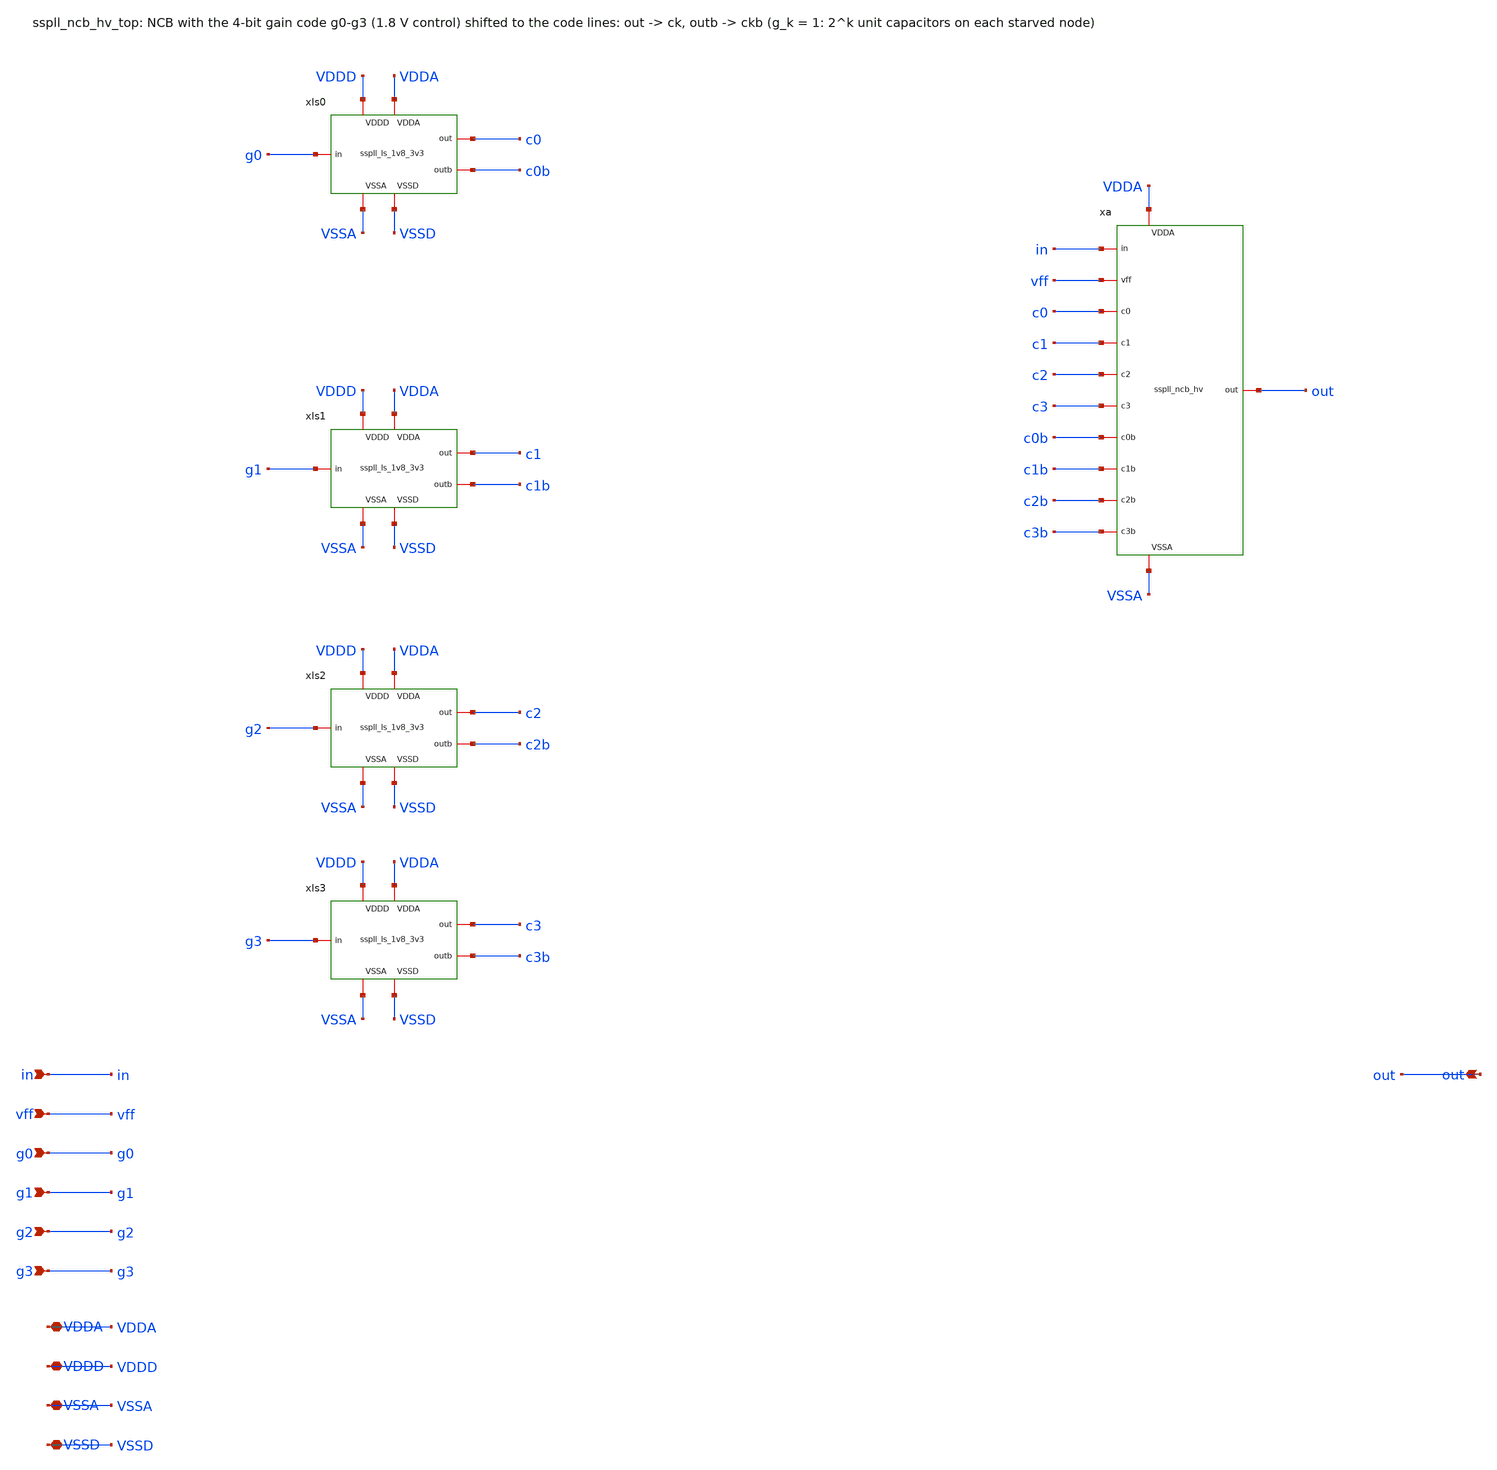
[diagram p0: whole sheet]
** sch_path: xschem/ncb_hv/sspll_ncb_hv_top.sch
**.subckt sspll_ncb_hv_top in vff g0 g1 g2 g3 out VDDA VDDD VSSA VSSD
*.ipin in
*.ipin vff
*.ipin g0
*.ipin g1
*.ipin g2
*.ipin g3
*.opin out
*.iopin VDDA
*.iopin VDDD
*.iopin VSSA
*.iopin VSSD
xls0 g0 c0 c0b VDDD VDDA VSSA VSSD sspll_ls_1v8_3v3
xls1 g1 c1 c1b VDDD VDDA VSSA VSSD sspll_ls_1v8_3v3
xls2 g2 c2 c2b VDDD VDDA VSSA VSSD sspll_ls_1v8_3v3
xls3 g3 c3 c3b VDDD VDDA VSSA VSSD sspll_ls_1v8_3v3
xa in vff c0 c1 c2 c3 c0b c1b c2b c3b out VDDA VSSA sspll_ncb_hv
**.ends

* expanding   symbol:  ../cco_hv/sspll_ls_1v8_3v3.sym # of pins=7
** sym_path: xschem/cco_hv/sspll_ls_1v8_3v3.sym
** sch_path: xschem/cco_hv/sspll_ls_1v8_3v3.sch
.subckt sspll_ls_1v8_3v3 in out outb VDDD VDDA VSSA VSSD
*.iopin VDDD
*.iopin VDDA
*.iopin VSSD
*.iopin VSSA
*.ipin in
*.opin outb
*.opin out
XXPI net1 in VDDD VDDD sky130_fd_pr__pfet_01v8 L=0.15 W=1 nf=1 ad='int((nf+1)/2) * W/nf * 0.29' as='int((nf+2)/2) * W/nf * 0.29'
+ pd='2*int((nf+1)/2) * (W/nf + 0.29)' ps='2*int((nf+2)/2) * (W/nf + 0.29)' nrd='0.29 / W' nrs='0.29 / W'
+ sa=0 sb=0 sd=0 mult=1 m=1
XXNI net1 in VSSD VSSD sky130_fd_pr__nfet_01v8 L=0.15 W=0.5 nf=1 ad='int((nf+1)/2) * W/nf * 0.29' as='int((nf+2)/2) * W/nf * 0.29'
+ pd='2*int((nf+1)/2) * (W/nf + 0.29)' ps='2*int((nf+2)/2) * (W/nf + 0.29)' nrd='0.29 / W' nrs='0.29 / W'
+ sa=0 sb=0 sd=0 mult=1 m=1
XXP1 net2 net3 VDDA VDDA sky130_fd_pr__pfet_g5v0d10v5 L=0.5 W=1 nf=1 ad='int((nf+1)/2) * W/nf * 0.29'
+ as='int((nf+2)/2) * W/nf * 0.29' pd='2*int((nf+1)/2) * (W/nf + 0.29)' ps='2*int((nf+2)/2) * (W/nf + 0.29)'
+ nrd='0.29 / W' nrs='0.29 / W' sa=0 sb=0 sd=0 mult=1 m=1
XXP2 net3 net2 VDDA VDDA sky130_fd_pr__pfet_g5v0d10v5 L=0.5 W=1 nf=1 ad='int((nf+1)/2) * W/nf * 0.29'
+ as='int((nf+2)/2) * W/nf * 0.29' pd='2*int((nf+1)/2) * (W/nf + 0.29)' ps='2*int((nf+2)/2) * (W/nf + 0.29)'
+ nrd='0.29 / W' nrs='0.29 / W' sa=0 sb=0 sd=0 mult=1 m=1
XXN1 net2 in VSSA VSSA sky130_fd_pr__nfet_g5v0d10v5 L=0.5 W=3 nf=1 ad='int((nf+1)/2) * W/nf * 0.29' as='int((nf+2)/2) * W/nf * 0.29'
+ pd='2*int((nf+1)/2) * (W/nf + 0.29)' ps='2*int((nf+2)/2) * (W/nf + 0.29)' nrd='0.29 / W' nrs='0.29 / W'
+ sa=0 sb=0 sd=0 mult=1 m=1
XXN2 net3 net1 VSSA VSSA sky130_fd_pr__nfet_g5v0d10v5 L=0.5 W=3 nf=1 ad='int((nf+1)/2) * W/nf * 0.29'
+ as='int((nf+2)/2) * W/nf * 0.29' pd='2*int((nf+1)/2) * (W/nf + 0.29)' ps='2*int((nf+2)/2) * (W/nf + 0.29)'
+ nrd='0.29 / W' nrs='0.29 / W' sa=0 sb=0 sd=0 mult=1 m=1
XXPB outb net3 VDDA VDDA sky130_fd_pr__pfet_g5v0d10v5 L=0.5 W=2 nf=1 ad='int((nf+1)/2) * W/nf * 0.29'
+ as='int((nf+2)/2) * W/nf * 0.29' pd='2*int((nf+1)/2) * (W/nf + 0.29)' ps='2*int((nf+2)/2) * (W/nf + 0.29)'
+ nrd='0.29 / W' nrs='0.29 / W' sa=0 sb=0 sd=0 mult=1 m=1
XXNB outb net3 VSSA VSSA sky130_fd_pr__nfet_g5v0d10v5 L=0.5 W=1 nf=1 ad='int((nf+1)/2) * W/nf * 0.29'
+ as='int((nf+2)/2) * W/nf * 0.29' pd='2*int((nf+1)/2) * (W/nf + 0.29)' ps='2*int((nf+2)/2) * (W/nf + 0.29)'
+ nrd='0.29 / W' nrs='0.29 / W' sa=0 sb=0 sd=0 mult=1 m=1
XXPO out net2 VDDA VDDA sky130_fd_pr__pfet_g5v0d10v5 L=0.5 W=2 nf=1 ad='int((nf+1)/2) * W/nf * 0.29'
+ as='int((nf+2)/2) * W/nf * 0.29' pd='2*int((nf+1)/2) * (W/nf + 0.29)' ps='2*int((nf+2)/2) * (W/nf + 0.29)'
+ nrd='0.29 / W' nrs='0.29 / W' sa=0 sb=0 sd=0 mult=1 m=1
XXNO out net2 VSSA VSSA sky130_fd_pr__nfet_g5v0d10v5 L=0.5 W=1 nf=1 ad='int((nf+1)/2) * W/nf * 0.29'
+ as='int((nf+2)/2) * W/nf * 0.29' pd='2*int((nf+1)/2) * (W/nf + 0.29)' ps='2*int((nf+2)/2) * (W/nf + 0.29)'
+ nrd='0.29 / W' nrs='0.29 / W' sa=0 sb=0 sd=0 mult=1 m=1
.ends


* expanding   symbol:  sspll_ncb_hv.sym # of pins=13
** sym_path: xschem/ncb_hv/sspll_ncb_hv.sym
** sch_path: xschem/ncb_hv/sspll_ncb_hv.sch
.subckt sspll_ncb_hv in vff c0 c1 c2 c3 c0b c1b c2b c3b out VDDA VSSA
*.ipin in
*.ipin vff
*.ipin c0
*.ipin c1
*.ipin c2
*.ipin c3
*.ipin c0b
*.ipin c1b
*.ipin c2b
*.ipin c3b
*.opin out
*.iopin VDDA
*.iopin VSSA
xb vff nb pd VDDA VSSA sspll_ncb_hv_bias
xl in nb pd c0 c1 c2 c3 c0b c1b c2b c3b out VDDA VSSA sspll_ncb_hv_line
.ends


* expanding   symbol:  sspll_ncb_hv_bias.sym # of pins=5
** sym_path: xschem/ncb_hv/sspll_ncb_hv_bias.sym
** sch_path: xschem/ncb_hv/sspll_ncb_hv_bias.sch
.subckt sspll_ncb_hv_bias vff nb pd VDDA VSSA
*.ipin vff
*.opin nb
*.opin pd
*.iopin VDDA
*.iopin VSSA
XXPD pd pd VDDA VDDA sky130_fd_pr__pfet_g5v0d10v5 L=0.5 W=4 nf=1 ad='int((nf+1)/2) * W/nf * 0.29' as='int((nf+2)/2) * W/nf * 0.29'
+ pd='2*int((nf+1)/2) * (W/nf + 0.29)' ps='2*int((nf+2)/2) * (W/nf + 0.29)' nrd='0.29 / W' nrs='0.29 / W'
+ sa=0 sb=0 sd=0 mult=1 m=1
XXI pd vff VSSA VSSA sky130_fd_pr__nfet_g5v0d10v5 L=1.0 W=2 nf=1 ad='int((nf+1)/2) * W/nf * 0.29' as='int((nf+2)/2) * W/nf * 0.29'
+ pd='2*int((nf+1)/2) * (W/nf + 0.29)' ps='2*int((nf+2)/2) * (W/nf + 0.29)' nrd='0.29 / W' nrs='0.29 / W'
+ sa=0 sb=0 sd=0 mult=1 m=1
XXPO nb pd VDDA VDDA sky130_fd_pr__pfet_g5v0d10v5 L=0.5 W=4 nf=1 ad='int((nf+1)/2) * W/nf * 0.29' as='int((nf+2)/2) * W/nf * 0.29'
+ pd='2*int((nf+1)/2) * (W/nf + 0.29)' ps='2*int((nf+2)/2) * (W/nf + 0.29)' nrd='0.29 / W' nrs='0.29 / W'
+ sa=0 sb=0 sd=0 mult=1 m=1
XXND nb nb VSSA VSSA sky130_fd_pr__nfet_g5v0d10v5 L=0.5 W=2 nf=1 ad='int((nf+1)/2) * W/nf * 0.29' as='int((nf+2)/2) * W/nf * 0.29'
+ pd='2*int((nf+1)/2) * (W/nf + 0.29)' ps='2*int((nf+2)/2) * (W/nf + 0.29)' nrd='0.29 / W' nrs='0.29 / W'
+ sa=0 sb=0 sd=0 mult=1 m=1
.ends


* expanding   symbol:  sspll_ncb_hv_line.sym # of pins=14
** sym_path: xschem/ncb_hv/sspll_ncb_hv_line.sym
** sch_path: xschem/ncb_hv/sspll_ncb_hv_line.sch
.subckt sspll_ncb_hv_line in nb pd c0 c1 c2 c3 c0b c1b c2b c3b out VDDA VSSA
*.opin out
*.ipin in
*.ipin nb
*.ipin pd
*.ipin c0
*.ipin c1
*.ipin c2
*.ipin c3
*.ipin c0b
*.ipin c1b
*.ipin c2b
*.ipin c3b
*.iopin VDDA
*.iopin VSSA
x1 net1 nb pd a VDDA VSSA sspll_ncb_hv_sinv
x2 a nb pd b VDDA VSSA sspll_ncb_hv_sinv
XX0P net1 in VDDA VDDA sky130_fd_pr__pfet_g5v0d10v5 L=0.5 W=2.5 nf=1 ad='int((nf+1)/2) * W/nf * 0.29'
+ as='int((nf+2)/2) * W/nf * 0.29' pd='2*int((nf+1)/2) * (W/nf + 0.29)' ps='2*int((nf+2)/2) * (W/nf + 0.29)'
+ nrd='0.29 / W' nrs='0.29 / W' sa=0 sb=0 sd=0 mult=1 m=1
XX0N net1 in VSSA VSSA sky130_fd_pr__nfet_g5v0d10v5 L=0.5 W=1 nf=1 ad='int((nf+1)/2) * W/nf * 0.29' as='int((nf+2)/2) * W/nf * 0.29'
+ pd='2*int((nf+1)/2) * (W/nf + 0.29)' ps='2*int((nf+2)/2) * (W/nf + 0.29)' nrd='0.29 / W' nrs='0.29 / W'
+ sa=0 sb=0 sd=0 mult=1 m=1
xba a c0 c1 c2 c3 c0b c1b c2b c3b VDDA VSSA sspll_ncb_hv_bank
xbb b c0 c1 c2 c3 c0b c1b c2b c3b VDDA VSSA sspll_ncb_hv_bank
XX3P out b VDDA VDDA sky130_fd_pr__pfet_g5v0d10v5 L=0.5 W=5 nf=1 ad='int((nf+1)/2) * W/nf * 0.29' as='int((nf+2)/2) * W/nf * 0.29'
+ pd='2*int((nf+1)/2) * (W/nf + 0.29)' ps='2*int((nf+2)/2) * (W/nf + 0.29)' nrd='0.29 / W' nrs='0.29 / W'
+ sa=0 sb=0 sd=0 mult=1 m=1
XX3N out b VSSA VSSA sky130_fd_pr__nfet_g5v0d10v5 L=0.5 W=2 nf=1 ad='int((nf+1)/2) * W/nf * 0.29' as='int((nf+2)/2) * W/nf * 0.29'
+ pd='2*int((nf+1)/2) * (W/nf + 0.29)' ps='2*int((nf+2)/2) * (W/nf + 0.29)' nrd='0.29 / W' nrs='0.29 / W'
+ sa=0 sb=0 sd=0 mult=1 m=1
.ends


* expanding   symbol:  sspll_ncb_hv_sinv.sym # of pins=6
** sym_path: xschem/ncb_hv/sspll_ncb_hv_sinv.sym
** sch_path: xschem/ncb_hv/sspll_ncb_hv_sinv.sch
.subckt sspll_ncb_hv_sinv i nb pd o VDDA VSSA
*.opin o
*.ipin i
*.ipin nb
*.ipin pd
*.iopin VDDA
*.iopin VSSA
XXSP net1 pd VDDA VDDA sky130_fd_pr__pfet_g5v0d10v5 L=0.5 W=4 nf=1 ad='int((nf+1)/2) * W/nf * 0.29' as='int((nf+2)/2) * W/nf * 0.29'
+ pd='2*int((nf+1)/2) * (W/nf + 0.29)' ps='2*int((nf+2)/2) * (W/nf + 0.29)' nrd='0.29 / W' nrs='0.29 / W'
+ sa=0 sb=0 sd=0 mult=30 m=30
XXP o i net1 VDDA sky130_fd_pr__pfet_g5v0d10v5 L=0.5 W=8 nf=1 ad='int((nf+1)/2) * W/nf * 0.29' as='int((nf+2)/2) * W/nf * 0.29'
+ pd='2*int((nf+1)/2) * (W/nf + 0.29)' ps='2*int((nf+2)/2) * (W/nf + 0.29)' nrd='0.29 / W' nrs='0.29 / W'
+ sa=0 sb=0 sd=0 mult=1 m=1
XXN o i net2 VSSA sky130_fd_pr__nfet_g5v0d10v5 L=0.5 W=3 nf=1 ad='int((nf+1)/2) * W/nf * 0.29' as='int((nf+2)/2) * W/nf * 0.29'
+ pd='2*int((nf+1)/2) * (W/nf + 0.29)' ps='2*int((nf+2)/2) * (W/nf + 0.29)' nrd='0.29 / W' nrs='0.29 / W'
+ sa=0 sb=0 sd=0 mult=1 m=1
XXS net2 nb VSSA VSSA sky130_fd_pr__nfet_g5v0d10v5 L=0.5 W=2 nf=1 ad='int((nf+1)/2) * W/nf * 0.29' as='int((nf+2)/2) * W/nf * 0.29'
+ pd='2*int((nf+1)/2) * (W/nf + 0.29)' ps='2*int((nf+2)/2) * (W/nf + 0.29)' nrd='0.29 / W' nrs='0.29 / W'
+ sa=0 sb=0 sd=0 mult=20 m=20
.ends


* expanding   symbol:  sspll_ncb_hv_bank.sym # of pins=11
** sym_path: xschem/ncb_hv/sspll_ncb_hv_bank.sym
** sch_path: xschem/ncb_hv/sspll_ncb_hv_bank.sch
.subckt sspll_ncb_hv_bank n c0 c1 c2 c3 c0b c1b c2b c3b VDDA VSSA
*.iopin n
*.iopin c0
*.iopin c1
*.iopin c2
*.iopin c3
*.iopin c0b
*.iopin c1b
*.iopin c2b
*.iopin c3b
*.iopin VDDA
*.iopin VSSA
XXSN0 n c0 net1 VSSA sky130_fd_pr__nfet_g5v0d10v5 L=0.5 W=0.5 nf=1 ad='int((nf+1)/2) * W/nf * 0.29' as='int((nf+2)/2) * W/nf * 0.29'
+ pd='2*int((nf+1)/2) * (W/nf + 0.29)' ps='2*int((nf+2)/2) * (W/nf + 0.29)' nrd='0.29 / W' nrs='0.29 / W'
+ sa=0 sb=0 sd=0 mult=1 m=1
XXSP0 net1 c0b n VDDA sky130_fd_pr__pfet_g5v0d10v5 L=0.5 W=0.5 nf=1 ad='int((nf+1)/2) * W/nf * 0.29'
+ as='int((nf+2)/2) * W/nf * 0.29' pd='2*int((nf+1)/2) * (W/nf + 0.29)' ps='2*int((nf+2)/2) * (W/nf + 0.29)'
+ nrd='0.29 / W' nrs='0.29 / W' sa=0 sb=0 sd=0 mult=1 m=1
XXC0 VSSA net1 VSSA VSSA sky130_fd_pr__nfet_g5v0d10v5 L=0.5 W=1 nf=1 ad='int((nf+1)/2) * W/nf * 0.29'
+ as='int((nf+2)/2) * W/nf * 0.29' pd='2*int((nf+1)/2) * (W/nf + 0.29)' ps='2*int((nf+2)/2) * (W/nf + 0.29)'
+ nrd='0.29 / W' nrs='0.29 / W' sa=0 sb=0 sd=0 mult=1 m=1
XXSN1 n c1 net2 VSSA sky130_fd_pr__nfet_g5v0d10v5 L=0.5 W=0.5 nf=1 ad='int((nf+1)/2) * W/nf * 0.29' as='int((nf+2)/2) * W/nf * 0.29'
+ pd='2*int((nf+1)/2) * (W/nf + 0.29)' ps='2*int((nf+2)/2) * (W/nf + 0.29)' nrd='0.29 / W' nrs='0.29 / W'
+ sa=0 sb=0 sd=0 mult=2 m=2
XXSP1 net2 c1b n VDDA sky130_fd_pr__pfet_g5v0d10v5 L=0.5 W=0.5 nf=1 ad='int((nf+1)/2) * W/nf * 0.29'
+ as='int((nf+2)/2) * W/nf * 0.29' pd='2*int((nf+1)/2) * (W/nf + 0.29)' ps='2*int((nf+2)/2) * (W/nf + 0.29)'
+ nrd='0.29 / W' nrs='0.29 / W' sa=0 sb=0 sd=0 mult=2 m=2
XXC1 VSSA net2 VSSA VSSA sky130_fd_pr__nfet_g5v0d10v5 L=0.5 W=1 nf=1 ad='int((nf+1)/2) * W/nf * 0.29'
+ as='int((nf+2)/2) * W/nf * 0.29' pd='2*int((nf+1)/2) * (W/nf + 0.29)' ps='2*int((nf+2)/2) * (W/nf + 0.29)'
+ nrd='0.29 / W' nrs='0.29 / W' sa=0 sb=0 sd=0 mult=2 m=2
XXSN2 n c2 net3 VSSA sky130_fd_pr__nfet_g5v0d10v5 L=0.5 W=0.5 nf=1 ad='int((nf+1)/2) * W/nf * 0.29' as='int((nf+2)/2) * W/nf * 0.29'
+ pd='2*int((nf+1)/2) * (W/nf + 0.29)' ps='2*int((nf+2)/2) * (W/nf + 0.29)' nrd='0.29 / W' nrs='0.29 / W'
+ sa=0 sb=0 sd=0 mult=4 m=4
XXSP2 net3 c2b n VDDA sky130_fd_pr__pfet_g5v0d10v5 L=0.5 W=0.5 nf=1 ad='int((nf+1)/2) * W/nf * 0.29'
+ as='int((nf+2)/2) * W/nf * 0.29' pd='2*int((nf+1)/2) * (W/nf + 0.29)' ps='2*int((nf+2)/2) * (W/nf + 0.29)'
+ nrd='0.29 / W' nrs='0.29 / W' sa=0 sb=0 sd=0 mult=4 m=4
XXC2 VSSA net3 VSSA VSSA sky130_fd_pr__nfet_g5v0d10v5 L=0.5 W=1 nf=1 ad='int((nf+1)/2) * W/nf * 0.29'
+ as='int((nf+2)/2) * W/nf * 0.29' pd='2*int((nf+1)/2) * (W/nf + 0.29)' ps='2*int((nf+2)/2) * (W/nf + 0.29)'
+ nrd='0.29 / W' nrs='0.29 / W' sa=0 sb=0 sd=0 mult=4 m=4
XXSN3 n c3 net4 VSSA sky130_fd_pr__nfet_g5v0d10v5 L=0.5 W=0.5 nf=1 ad='int((nf+1)/2) * W/nf * 0.29' as='int((nf+2)/2) * W/nf * 0.29'
+ pd='2*int((nf+1)/2) * (W/nf + 0.29)' ps='2*int((nf+2)/2) * (W/nf + 0.29)' nrd='0.29 / W' nrs='0.29 / W'
+ sa=0 sb=0 sd=0 mult=8 m=8
XXSP3 net4 c3b n VDDA sky130_fd_pr__pfet_g5v0d10v5 L=0.5 W=0.5 nf=1 ad='int((nf+1)/2) * W/nf * 0.29'
+ as='int((nf+2)/2) * W/nf * 0.29' pd='2*int((nf+1)/2) * (W/nf + 0.29)' ps='2*int((nf+2)/2) * (W/nf + 0.29)'
+ nrd='0.29 / W' nrs='0.29 / W' sa=0 sb=0 sd=0 mult=8 m=8
XXC3 VSSA net4 VSSA VSSA sky130_fd_pr__nfet_g5v0d10v5 L=0.5 W=1 nf=1 ad='int((nf+1)/2) * W/nf * 0.29'
+ as='int((nf+2)/2) * W/nf * 0.29' pd='2*int((nf+1)/2) * (W/nf + 0.29)' ps='2*int((nf+2)/2) * (W/nf + 0.29)'
+ nrd='0.29 / W' nrs='0.29 / W' sa=0 sb=0 sd=0 mult=8 m=8
.ends

.end
